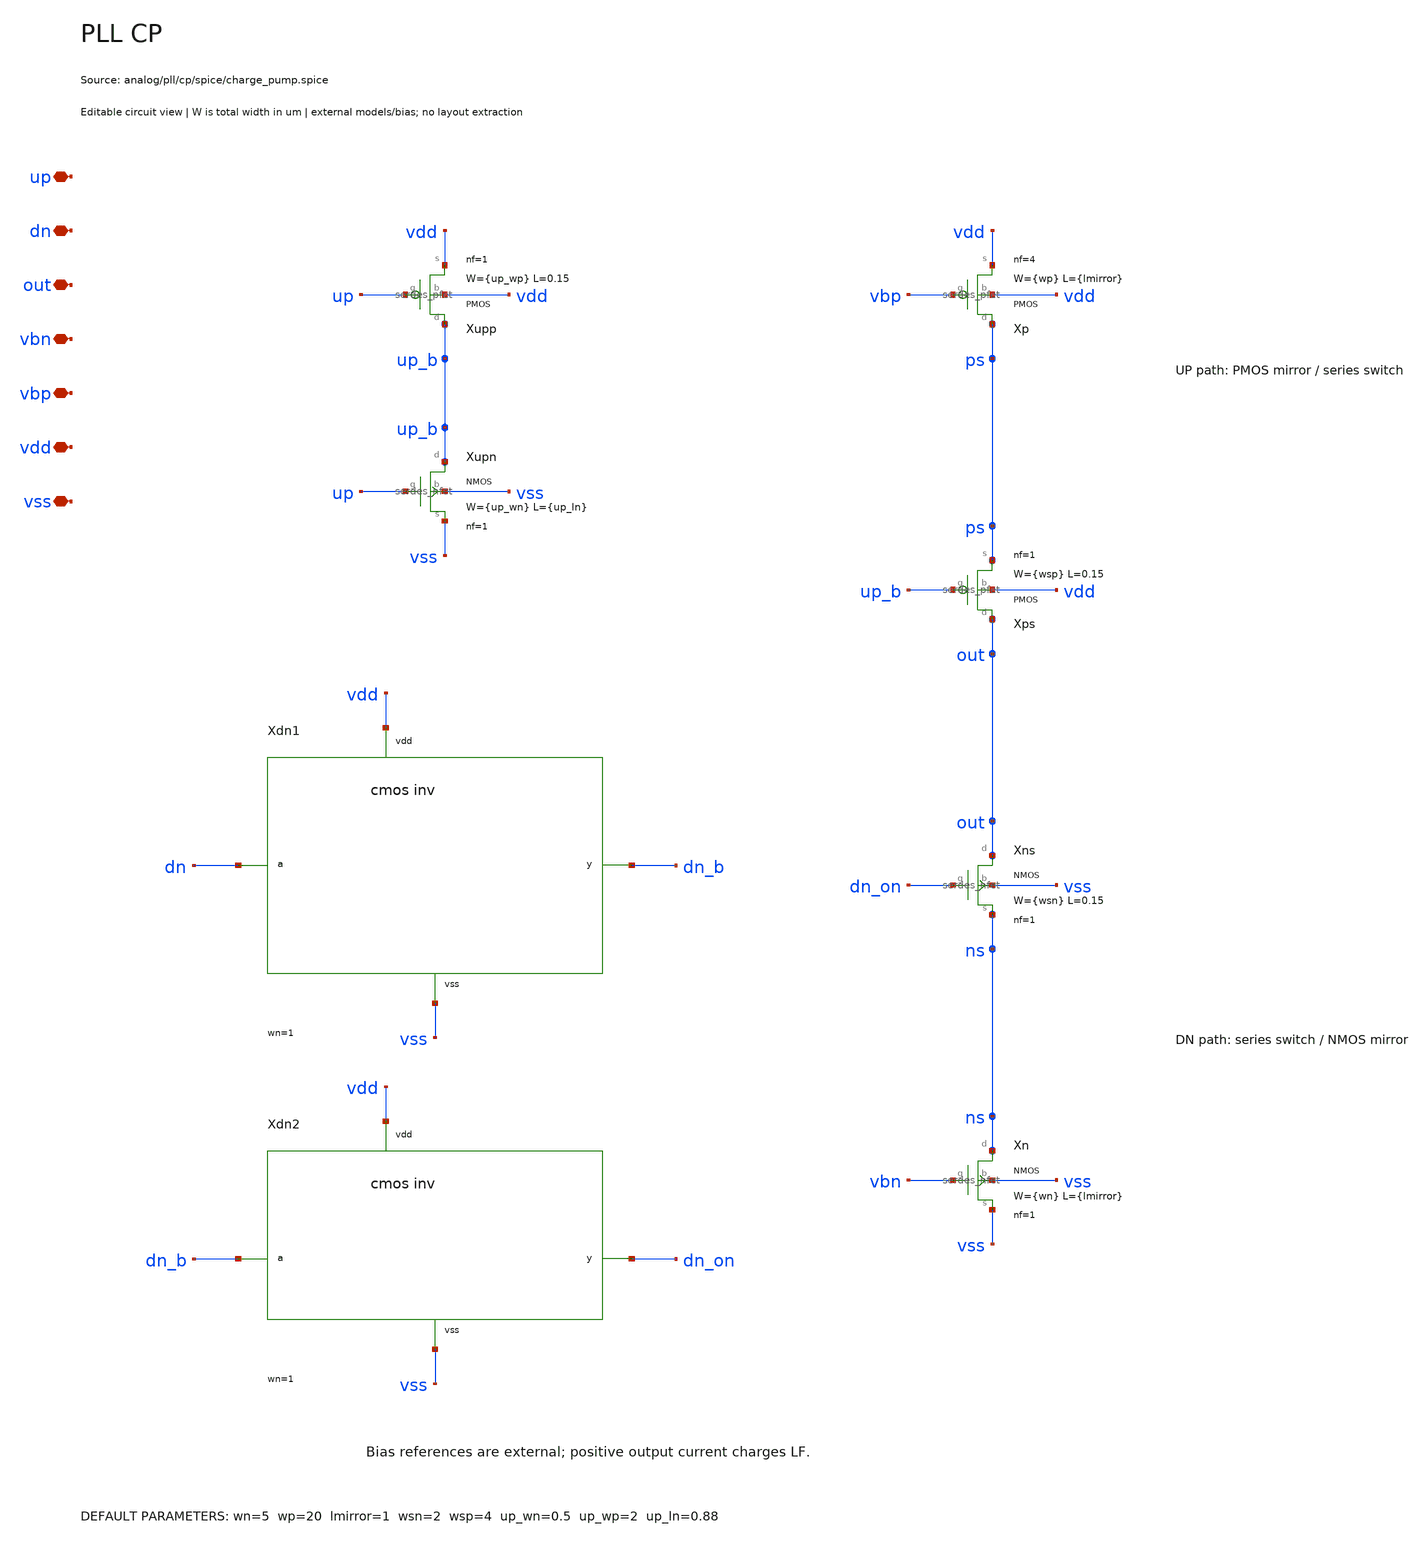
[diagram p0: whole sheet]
** sch_path: analog/pll/cp/schematic/pll_cp.sch
**.subckt pll_cp up dn out vbn vbp vdd vss
*.iopin up
*.iopin dn
*.iopin out
*.iopin vbn
*.iopin vbp
*.iopin vdd
*.iopin vss
Xupn up_b up vss vss serdes_nfet w={up_wn} l={up_ln} nf=1
Xupp up_b up vdd vdd serdes_pfet w={up_wp} l=0.15 nf=1
Xdn1 dn dn_b vdd vss serdes_cmos_inv wn=1 wp=2
Xdn2 dn_b dn_on vdd vss serdes_cmos_inv wn=1 wp=2
Xp ps vbp vdd vdd serdes_pfet w={wp} l={lmirror} nf=4
Xps out up_b ps vdd serdes_pfet w={wsp} l=0.15 nf=1
Xns out dn_on ns vss serdes_nfet w={wsn} l=0.15 nf=1
Xn ns vbn vss vss serdes_nfet w={wn} l={lmirror} nf=1
**.ends

* expanding   symbol:  serdes/serdes_nfet.sym # of pins=4
** sym_path: analog/common/devices/schematic/serdes_nfet.sym
** sch_path: analog/common/devices/schematic/serdes_nfet.sch
.subckt serdes_nfet d g s b  w=1 l=0.15 nf=1
*.iopin d
*.iopin g
*.iopin s
*.iopin b
Xmos d g s b sky130_fd_pr__nfet_01v8 w={w} l={l} nf={nf} ad={floor((nf+1)/2)*(w/nf)*0.29} as={floor((nf+2)/2)*(w/nf)*0.29}
+ pd={2*floor((nf+1)/2)*(w/nf+0.29)} ps={2*floor((nf+2)/2)*(w/nf+0.29)}
.ends


* expanding   symbol:  serdes/serdes_pfet.sym # of pins=4
** sym_path: analog/common/devices/schematic/serdes_pfet.sym
** sch_path: analog/common/devices/schematic/serdes_pfet.sch
.subckt serdes_pfet d g s b  w=3 l=0.15 nf=1
*.iopin d
*.iopin g
*.iopin s
*.iopin b
Xmos d g s b sky130_fd_pr__pfet_01v8 w={w} l={l} nf={nf} ad={floor((nf+1)/2)*(w/nf)*0.29} as={floor((nf+2)/2)*(w/nf)*0.29}
+ pd={2*floor((nf+1)/2)*(w/nf+0.29)} ps={2*floor((nf+2)/2)*(w/nf+0.29)}
.ends


* expanding   symbol:  serdes/serdes_cmos_inv.sym # of pins=4
** sym_path: analog/common/devices/schematic/serdes_cmos_inv.sym
** sch_path: analog/common/devices/schematic/serdes_cmos_inv.sch
.subckt serdes_cmos_inv a y vdd vss  wn=1 wp=2
*.iopin a
*.iopin y
*.iopin vdd
*.iopin vss
Xn y a vss vss serdes_nfet w={wn} l=0.15 nf=1
Xp y a vdd vdd serdes_pfet w={wp} l=0.15 nf=1
.ends

.end
